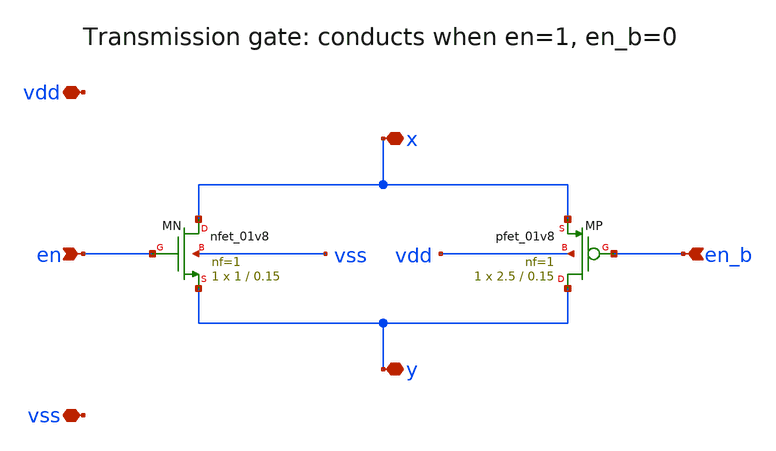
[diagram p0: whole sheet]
** sch_path: lab5/xschem/tgate.sch
**.subckt tgate x y en en_b vdd vss
*.iopin x
*.iopin y
*.ipin en
*.ipin en_b
*.iopin vdd
*.iopin vss
XMN x en y vss sky130_fd_pr__nfet_01v8 L=0.15 W=1 nf=1 ad='int((1 + 1)/2) * 1 / 1 * 0.29' as='int((1 + 2)/2) * 1 / 1 * 0.29'
+ pd='2*int((1 + 1)/2) * (1 / 1 + 0.29)' ps='2*int((1 + 2)/2) * (1 / 1 + 0.29)' nrd='0.29 / 1 ' nrs='0.29 / 1 '
+ sa=0 sb=0 sd=0 mult=1 m=1
XMP y en_b x vdd sky130_fd_pr__pfet_01v8 L=0.15 W=2.5 nf=1 ad='int((nf+1)/2) * W/nf * 0.29' as='int((nf+2)/2) * W/nf * 0.29'
+ pd='2*int((nf+1)/2) * (W/nf + 0.29)' ps='2*int((nf+2)/2) * (W/nf + 0.29)' nrd='0.29 / W' nrs='0.29 / W'
+ sa=0 sb=0 sd=0 mult=1 m=1
**.ends
.end
